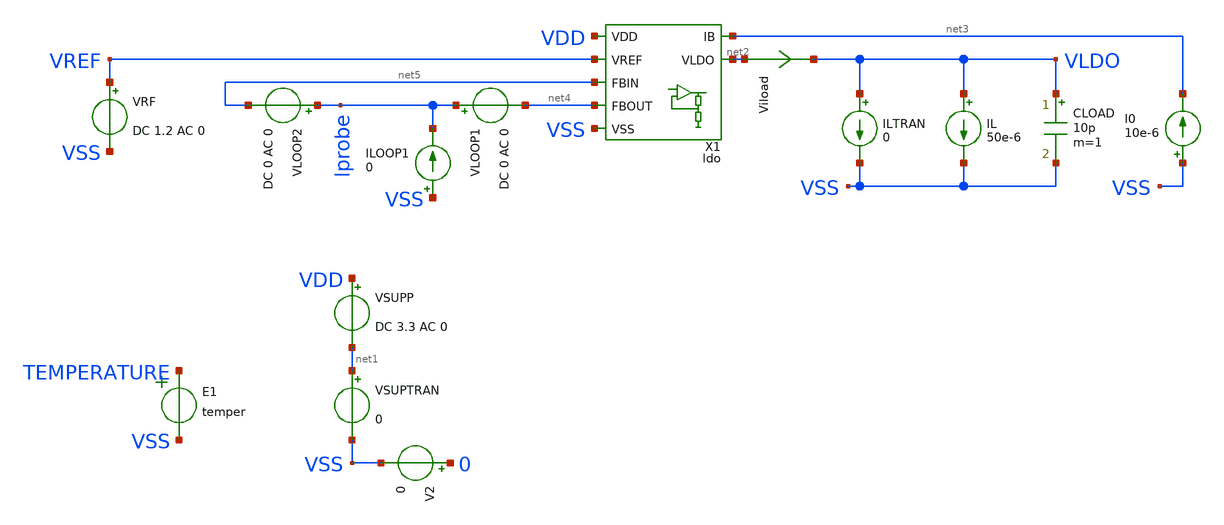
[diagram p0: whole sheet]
** sch_path: ip/ldo/xschem/ldo_tb.sch
**.subckt ldo_tb
VSUPP VDD net1 DC 3.3 AC 0
V2 0 VSS 0
E1 TEMPERATURE VSS VOL=' temper '
I0 VSS net3 10e-6
CLOAD VLDO VSS 10p m=1
VRF VREF VSS DC 1.2 AC 0
IL VLDO VSS 50e-6
VSUPTRAN net1 VSS 0
ILTRAN VLDO VSS 0
Viload net2 VLDO 0
.save i(viload)
VLOOP1 lprobe net4 DC 0 AC 0
VLOOP2 lprobe net5 DC 0 AC 0
ILOOP1 VSS lprobe 0
X1 VDD VSS net3 VREF net2 net5 net4 ldo
**** begin user architecture code

.csparam TB_ID=${::TB_ID}
.csparam MC_RUNS=${::MC_RUNS}
.csparam EXIT_NGSPICE=${::EXIT_NGSPICE}
.lib ${::IHP_MODELS}/sg13g2.lib ${::CORNER}


* this experimental option enables mos model bin
* selection based on W/NF instead of W
.option wnflag=0

.control
option savecurrents
save all


* dummy block for goto
if (1)
if TB_ID = 0
	goto AC_LOOPGAIN
end
if TB_ID = 1
	goto TRAN_CURVE_TEMP
end
if TB_ID = 2
	goto TRAN_CURVE_VDD
end
if TB_ID = 3
	goto TRAN_CURVE_ILOAD
end
if TB_ID = 4
	goto VLDO_NOISE
end
if TB_ID = 5
	goto AC_PSRR
end
if TB_ID = 6
	goto TRAN_LINE
end
if TB_ID = 7
	goto TRAN_LOAD
end
if TB_ID = 8
	goto AC_LOOPGAIN
end

****************************************
label TRAN_CURVE_TEMP
save all
****************************************
if MC_RUNS = 0
	let veclen=3
	let vldo_pp = vector(veclen)
	let vldo_t20 = vector(veclen)
	let vldo_tc20 = vector(veclen)
	let vldo_mean = vector(veclen)
	let vsup = vector(veclen)
	let isup = vector(veclen)
	let run = 0

	foreach v_sweep 1.8 2.5 3.3
	*foreach v_sweep 3.3

		.include ldo_tran_curve_temp_ops.inc

		reset
		let run = run + 1
	end

	set nobreak
	set width=300
	print isup, vsup, vldo_pp, vldo_mean, vldo_t20, vldo_tc20 > ldo_tran_temp.csv

else
	let vldo_pp = vector(MC_RUNS)
	let vldo_t20 = vector(MC_RUNS)
	let vldo_tc20 = vector(MC_RUNS)
	let vldo_mean = vector(MC_RUNS)
	let vsup = vector(MC_RUNS)
	let isup = vector(MC_RUNS)
	let run = 0
	set v_sweep = 3.3

	dowhile run < MC_RUNS
		echo MC-RUN: $&run

		.include ldo_tran_curve_temp_ops.inc

 		reset
		let run = run + 1
	end

	set nobreak
	set width=300
	print isup, vsup, vldo_pp, vldo_mean, vldo_t20, vldo_tc20 > ldo_tran_temp.csv
end
goto done

****************************************
label TRAN_CURVE_VDD
save all
****************************************
if MC_RUNS = 0
	let veclen=3
	let vldo_pp = vector(veclen)
	let vldo_3v3 = vector(veclen)
	let vldo_tc3v3 = vector(veclen)
	let vldo_mean = vector(veclen)
	let te = vector(veclen)
	let isup = vector(veclen)
	let run = 0

	foreach t_sweep -40 20 125
	*foreach t_sweep 20

		.include ldo_tran_curve_vdd_ops.inc

		let run = run + 1
	end

	set nobreak
	set width=300
	print isup, te, vldo_pp, vldo_mean, vldo_3v3, vldo_tc3v3 > ldo_tran_vdd.csv

else
	let vldo_pp = vector(MC_RUNS)
	let vldo_3v3 = vector(MC_RUNS)
	let vldo_tc3v3 = vector(MC_RUNS)
	let vldo_mean = vector(MC_RUNS)
	let te = vector(MC_RUNS)
	let isup = vector(MC_RUNS)
	let run = 0
	set t_sweep = 20

	dowhile run < MC_RUNS
		echo MC-RUN: $&run

		.include ldo_tran_curve_vdd_ops.inc

 		reset
		let run = run + 1
	end

	set nobreak
	set width=300
	print isup, te, vldo_pp, vldo_mean, vldo_3v3, vldo_tc3v3 > ldo_tran_vdd.csv
end
goto done

****************************************
label TRAN_CURVE_ILOAD
save all
****************************************
if MC_RUNS = 0
	let veclen=3
	let vldo_pp = vector(veclen)
	let vldo_100u = vector(veclen)
	let vldo_tc100u = vector(veclen)
	let vldo_mean = vector(veclen)
	let te = vector(veclen)
	let isup = vector(veclen)
	let run = 0

	foreach t_sweep -40 20 125
	*foreach t_sweep 20

		.include ldo_tran_curve_iload_ops.inc

		reset
		let run = run + 1
	end

	set nobreak
	set width=300
	print isup, te, vldo_pp, vldo_mean, vldo_100u, vldo_tc100u > ldo_tran_iload.csv

else
	let vldo_pp = vector(MC_RUNS)
	let vldo_100u = vector(MC_RUNS)
	let vldo_tc100u = vector(MC_RUNS)
	let vldo_mean = vector(MC_RUNS)
	let te = vector(MC_RUNS)
	let isup = vector(MC_RUNS)
	let run = 0
	set t_sweep = 20

	dowhile run < MC_RUNS
		echo MC-RUN: $&run

		.include ldo_tran_curve_iload_ops.inc

 		reset
		let run = run + 1
	end

	set nobreak
	set width=300
	print isup, te, vldo_pp, vldo_mean, vldo_100u, vldo_tc100u > ldo_tran_iload.csv
end
goto done

****************************************
label VLDO_NOISE
****************************************
noise v(vldo) VSUPP dec 10 1 100e3 1
setplot noise2
print onoise_total
setplot noise1
if EXIT_NGSPICE = 0
	plot onoise_spectrum
end
write ldo_ac_noise.raw all

* https://sourceforge.net/p/ngspice/discussion/120973/thread/2aa3e30f/ -- Holger Vogt
* script to read a specific y-value if x given
**********************************************
let f0 = vector(1)
let f1 = vector(1)
let n_f0 = vector(1)
let n_f1 = vector(1)
compose freq_list values 10 10e3
foreach freq_idx 0 1
	let freq = freq_list[$freq_idx]
	* find index where freqency is just above interesting value
	setplot noise1
	let nn = 0
	while frequency[nn] < freq
		let nn = nn + 1
	end
	* define vectors of frequncies and values just above and below
	* selected frequeny
	let fnn = frequency[nn]
	let nn1 = nn - 1
	let fnn1 = frequency[nn1]
	let snn = onoise_spectrum[nn]
	let snn1 = onoise_spectrum[nn1]
	*print vector values
	echo nn = $&nn  fnn = $&fnn  snn = $&snn
	echo nn1 = $&nn1  fnn1 = $&fnn1  snn1 = $&snn1
	*linear interpolation for exact frequency
	let newsnn = snn1 + (snn - snn1)/(fnn - fnn1)*(freq - fnn1)
	echo newfnn = $&freq  newsnn = $&newsnn
	if $freq_idx = 0
		let f0 = freq
		let n_f0 = newsnn
	end
	if $freq_idx = 1
		let f1 = freq
		let n_f1 = newsnn
	end
end
set nobreak
set width=300
set noprintscale
print col f0, n_f0, f1, n_f1 > ldo_ac_noise.csv

goto done

****************************************
label AC_PSRR
save all
****************************************
if MC_RUNS = 0
	let psrr_p_10Hz = vector(MC_RUNS+1)
	let psrr_p_10MHz = vector(MC_RUNS+1)
	let run=0

	.include ldo_ac_psrr_ops.inc

	set nobreak
	set width=300
	print col psrr_p_10Hz, psrr_p_10MHz > ldo_ac_psrr.csv
else
	let psrr_p_10Hz = vector(MC_RUNS)
	let psrr_p_10MHz = vector(MC_RUNS)
	let run=0
	dowhile run < MC_RUNS
		echo MC-RUN: $&run

		.include ldo_ac_psrr_ops.inc

 		reset
		let run = run + 1
	end
	set nobreak
	set width=300
	print psrr_p_10Hz, psrr_p_10MHz > ldo_ac_psrr.csv
end
goto done

****************************************
label TRAN_LINE
save all
****************************************
if MC_RUNS = 0
	let line_tran_pp = vector(MC_RUNS+1)
	let run=0

	.include ldo_tran_line_ops.inc

	set nobreak
	set width=300
	print col line_tran_pp > ldo_tran_line.csv
else
	let line_tran_pp = vector(MC_RUNS)
	let run=0
	dowhile run < MC_RUNS
		echo MC-RUN: $&run

		.include ldo_tran_line_ops.inc

 		reset
		let run = run + 1
	end
	set nobreak
	set width=300
	print line_tran_pp > ldo_tran_line.csv
end
goto done

****************************************
label TRAN_LOAD
save all
****************************************
if MC_RUNS = 0
	let load_tran_pp = vector(MC_RUNS+1)
	let run=0

	.include ldo_tran_load_ops.inc

	set nobreak
	set width=300
	print col load_tran_pp > ldo_tran_load.csv
else
	let load_tran_pp = vector(MC_RUNS)
	let run=0
	dowhile run < MC_RUNS
		echo MC-RUN: $&run

		.include ldo_tran_load_ops.inc

 		reset
		let run = run + 1
	end
	set nobreak
	set width=300
	print load_tran_pp > ldo_tran_load.csv
end
goto done

****************************************
label AC_LOOPGAIN
save all
****************************************
if MC_RUNS = 0
	let loop_pm = vector(MC_RUNS+1)
	let run = 0

	.include ldo_ac_loopgain_ops.inc

	set nobreak
	set width=300
	print col loop_pm > ldo_ac_loop.csv

else
	let loop_pm = vector(MC_RUNS)
	let run = 0

	dowhile run < MC_RUNS
		echo MC-RUN: $&run

		.include ldo_ac_loopgain_ops.inc

 		reset
		let run = run + 1
	end

	set nobreak
	set width=300
	print col loop_pm > ldo_ac_loop.csv
end
goto done

****************************************
label done
****************************************
if EXIT_NGSPICE > 0.0
	exit
end
end
.endc


**** end user architecture code
**.ends

* expanding   symbol:  ldo.sym # of pins=7
** sym_path: ip/ldo/xschem/ldo.sym
** sch_path: ip/ldo/xschem/ldo.sch
.subckt ldo VDD VSS IB VREF VLDO FBIN FBOUT
*.iopin VSS
*.iopin VDD
*.opin VLDO
*.ipin VREF
*.opin FBOUT
*.ipin FBIN
*.ipin IB
X1 VDD VSS VLDO IB FBIN VREF ldoota
XRT VLDO FBOUT VSS rhigh w=0.5e-6 l=12.5e-6 m=1 b=0 mm_ok=1
XRB FBOUT VSS VSS rhigh w=0.5e-6 l=50e-6 m=1 b=0 mm_ok=1
.ends


* expanding   symbol:  ldoota.sym # of pins=6
** sym_path: ip/ldo/xschem/ldoota.sym
** sch_path: ip/ldo/xschem/ldoota.sch
.subckt ldoota VDD VSS VOUT IB INN INP
*.ipin IB
*.iopin VDD
*.iopin VSS
*.iopin INP
*.iopin INN
*.iopin VOUT
XMMIRL1 net4 net1 VDD VDD sg13_hv_pmos w=10u l=2u ng=1 m=2 mm_ok=1
XMMIRR net2 net2 VDD VDD sg13_hv_pmos w=10u l=2u ng=1 m=2 mm_ok=1
XMMIRL net1 net1 VDD VDD sg13_hv_pmos w=10u l=2u ng=1 m=2 mm_ok=1
XMO vot net2 VDD VDD sg13_hv_pmos w=10u l=2u ng=1 m=10 mm_ok=1
XMOT VOUT vot VDD VDD sg13_hv_pmos w=10u l=0.5u ng=1 m=40 mm_ok=1
XMDL net1 INP net3 VSS sg13_hv_nmos w=10u l=2u ng=1 m=10 mm_ok=1
XMDR net2 INN net3 VSS sg13_hv_nmos w=10u l=2u ng=1 m=10 mm_ok=1
XMMIR2 net3 IB VSS VSS sg13_hv_nmos w=10u l=2u ng=1 m=2 mm_ok=1
XMOB VOUT IB VSS VSS sg13_hv_nmos w=10u l=2u ng=1 m=8 mm_ok=1
XMMIR3 vot net4 VSS VSS sg13_hv_nmos w=10u l=2u ng=1 m=10 mm_ok=1
XMMIRL2 net4 net4 VSS VSS sg13_hv_nmos w=10u l=2u ng=1 m=2 mm_ok=1
XMMIR1 IB IB VSS VSS sg13_hv_nmos w=10u l=2u ng=1 m=2 mm_ok=1
XR1 VOUT net5 VSS rppd w=1e-6 l=10.6e-6 m=1 b=0 mm_ok=1
XC1 net5 vot cap_cmim w=24e-6 l=24e-6 m=9 mm_ok=1
.ends

.end
